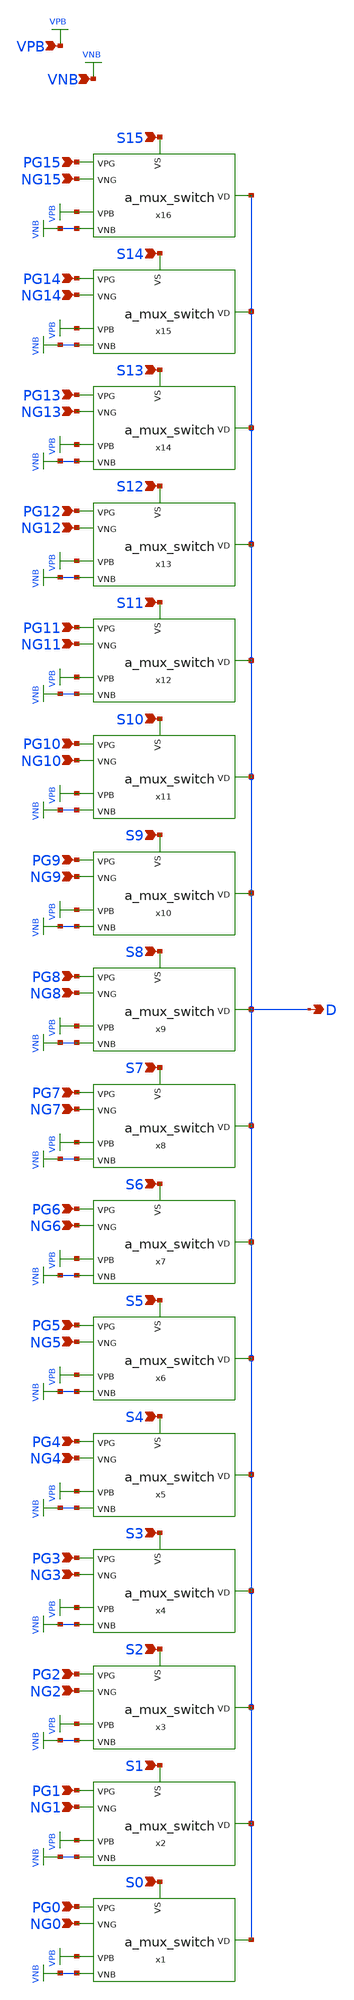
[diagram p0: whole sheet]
** sch_path: analog_mux_files 2/switch_x16.sch
**.subckt switch_x16 PG0 NG0 S0 PG1 NG1 S1 PG2 NG2 S2 PG3 NG3 S3 PG4 NG4 S4 PG5 NG5 S5 PG6 NG6 S6
*+ PG7 NG7 S7 PG8 NG8 S8 PG9 NG9 S9 PG10 NG10 S10 PG11 NG11 S11 PG12 NG12 S12 PG13 NG13 S13 PG14 NG14 S14
*+ PG15 NG15 S15 D VPB VNB
*.ipin PG0
*.ipin NG0
*.ipin S0
*.ipin PG1
*.ipin NG1
*.ipin S1
*.ipin PG2
*.ipin NG2
*.ipin S2
*.ipin PG3
*.ipin NG3
*.ipin S3
*.ipin PG4
*.ipin NG4
*.ipin S4
*.ipin PG5
*.ipin NG5
*.ipin S5
*.ipin PG6
*.ipin NG6
*.ipin S6
*.ipin PG7
*.ipin NG7
*.ipin S7
*.ipin PG8
*.ipin NG8
*.ipin S8
*.ipin PG9
*.ipin NG9
*.ipin S9
*.ipin PG10
*.ipin NG10
*.ipin S10
*.ipin PG11
*.ipin NG11
*.ipin S11
*.ipin PG12
*.ipin NG12
*.ipin S12
*.ipin PG13
*.ipin NG13
*.ipin S13
*.ipin PG14
*.ipin NG14
*.ipin S14
*.ipin PG15
*.ipin NG15
*.ipin S15
*.opin D
*.ipin VPB
*.ipin VNB
x1 VNB NG0 VPB PG0 S0 D a_mux_switch
x2 VNB NG1 VPB PG1 S1 D a_mux_switch
x3 VNB NG2 VPB PG2 S2 D a_mux_switch
x4 VNB NG3 VPB PG3 S3 D a_mux_switch
x5 VNB NG4 VPB PG4 S4 D a_mux_switch
x6 VNB NG5 VPB PG5 S5 D a_mux_switch
x7 VNB NG6 VPB PG6 S6 D a_mux_switch
x8 VNB NG7 VPB PG7 S7 D a_mux_switch
x9 VNB NG8 VPB PG8 S8 D a_mux_switch
x10 VNB NG9 VPB PG9 S9 D a_mux_switch
x11 VNB NG10 VPB PG10 S10 D a_mux_switch
x12 VNB NG11 VPB PG11 S11 D a_mux_switch
x13 VNB NG12 VPB PG12 S12 D a_mux_switch
x14 VNB NG13 VPB PG13 S13 D a_mux_switch
x15 VNB NG14 VPB PG14 S14 D a_mux_switch
x16 VNB NG15 VPB PG15 S15 D a_mux_switch
**.ends

* expanding   symbol:  analog_mux_files/a_mux_switch.sym # of pins=6
** sym_path: analog_mux_files 2/a_mux_switch.sym
** sch_path: analog_mux_files 2/a_mux_switch.sch
.subckt a_mux_switch VNB VNG VPB VPG VS VD
*.ipin VPG
*.ipin VNG
*.ipin VS
*.opin VD
*.ipin VPB
*.ipin VNB
XM1 VD VPG VS VPB sky130_fd_pr__pfet_01v8 L=0.15 W=20 nf=1 ad='int((nf+1)/2) * W/nf * 0.29' as='int((nf+2)/2) * W/nf * 0.29'
+ pd='2*int((nf+1)/2) * (W/nf + 0.29)' ps='2*int((nf+2)/2) * (W/nf + 0.29)' nrd='0.29 / W' nrs='0.29 / W'
+ sa=0 sb=0 sd=0 mult=1 m=1
XM2 VD VNG VS VNB sky130_fd_pr__nfet_01v8 L=0.15 W=20 nf=1 ad='int((nf+1)/2) * W/nf * 0.29' as='int((nf+2)/2) * W/nf * 0.29'
+ pd='2*int((nf+1)/2) * (W/nf + 0.29)' ps='2*int((nf+2)/2) * (W/nf + 0.29)' nrd='0.29 / W' nrs='0.29 / W'
+ sa=0 sb=0 sd=0 mult=1 m=1
.ends

.GLOBAL VPB
.GLOBAL VNB
.end
